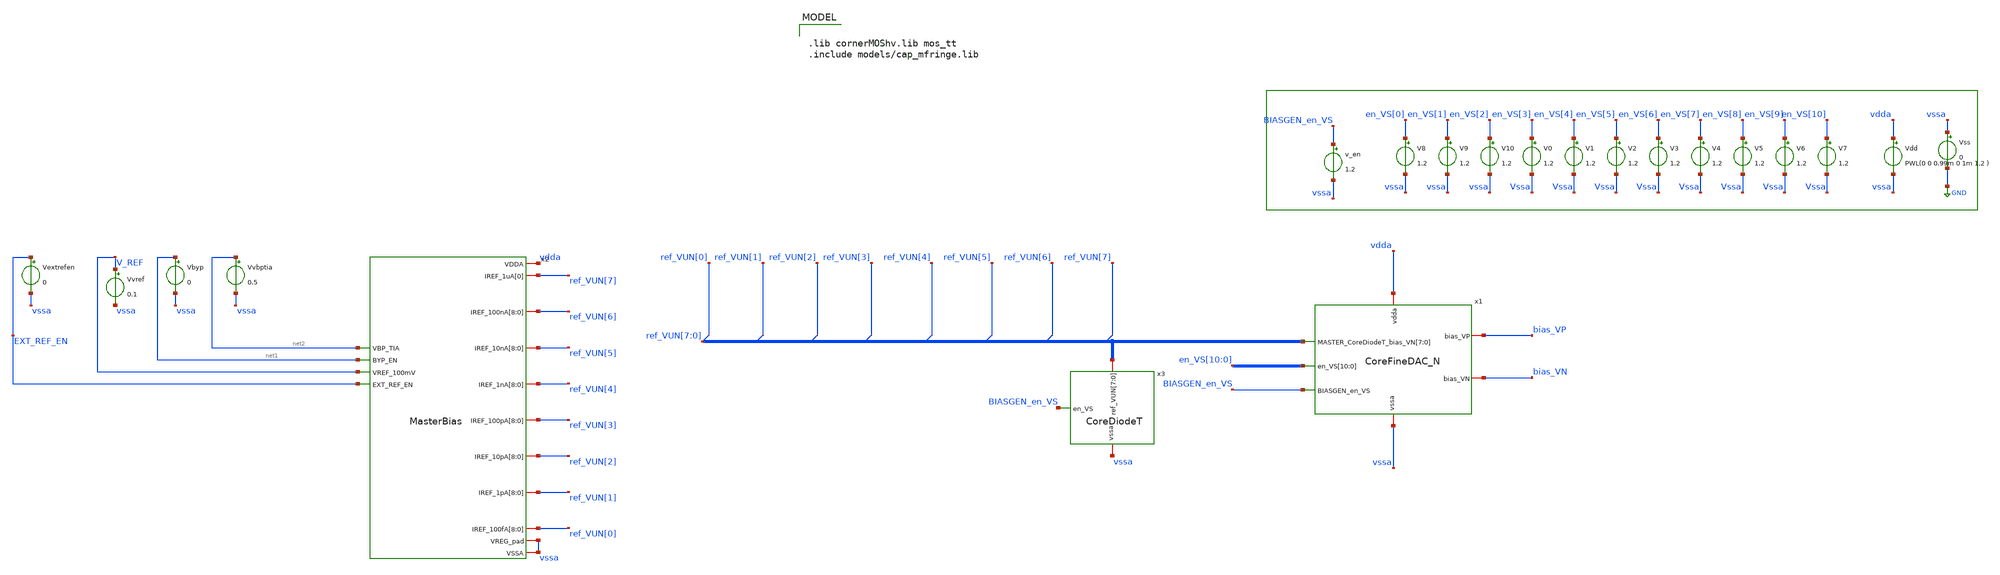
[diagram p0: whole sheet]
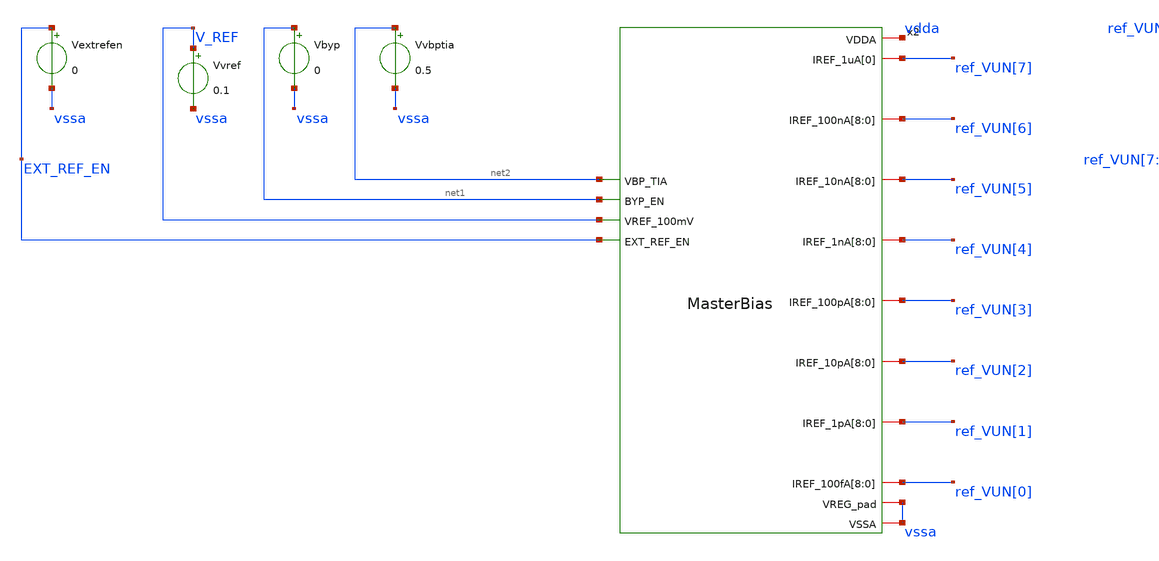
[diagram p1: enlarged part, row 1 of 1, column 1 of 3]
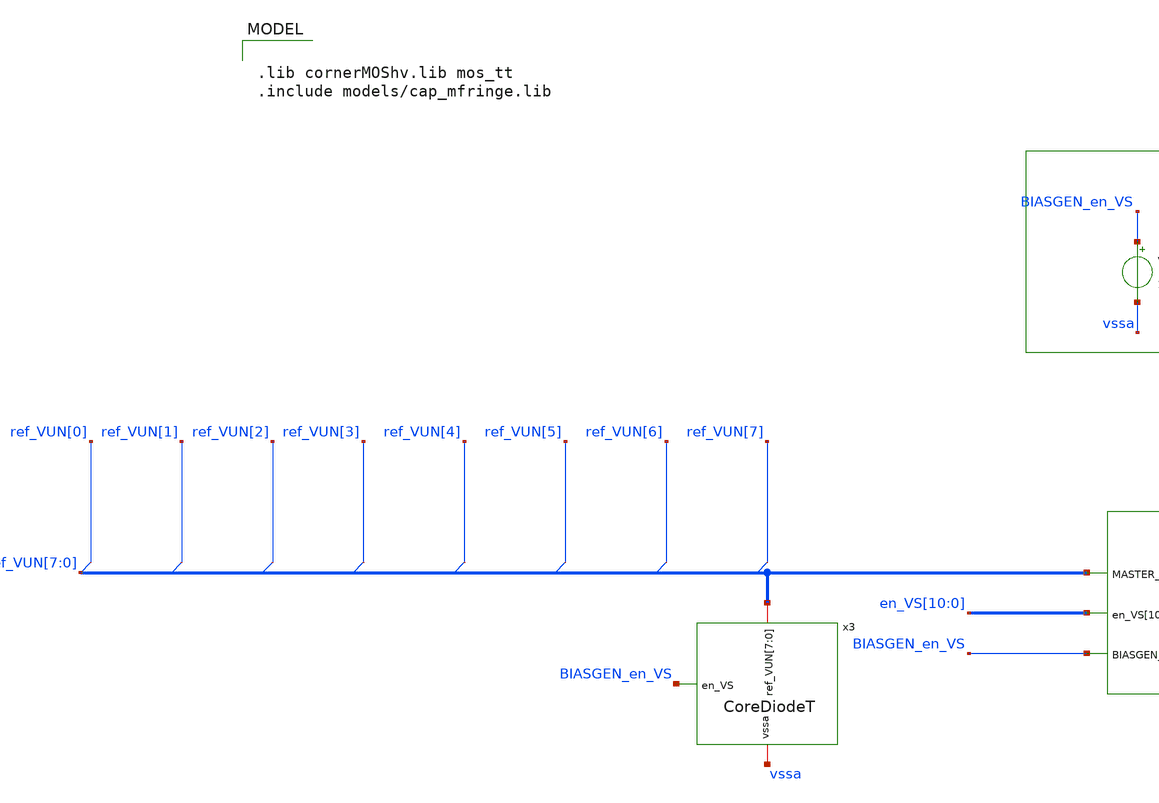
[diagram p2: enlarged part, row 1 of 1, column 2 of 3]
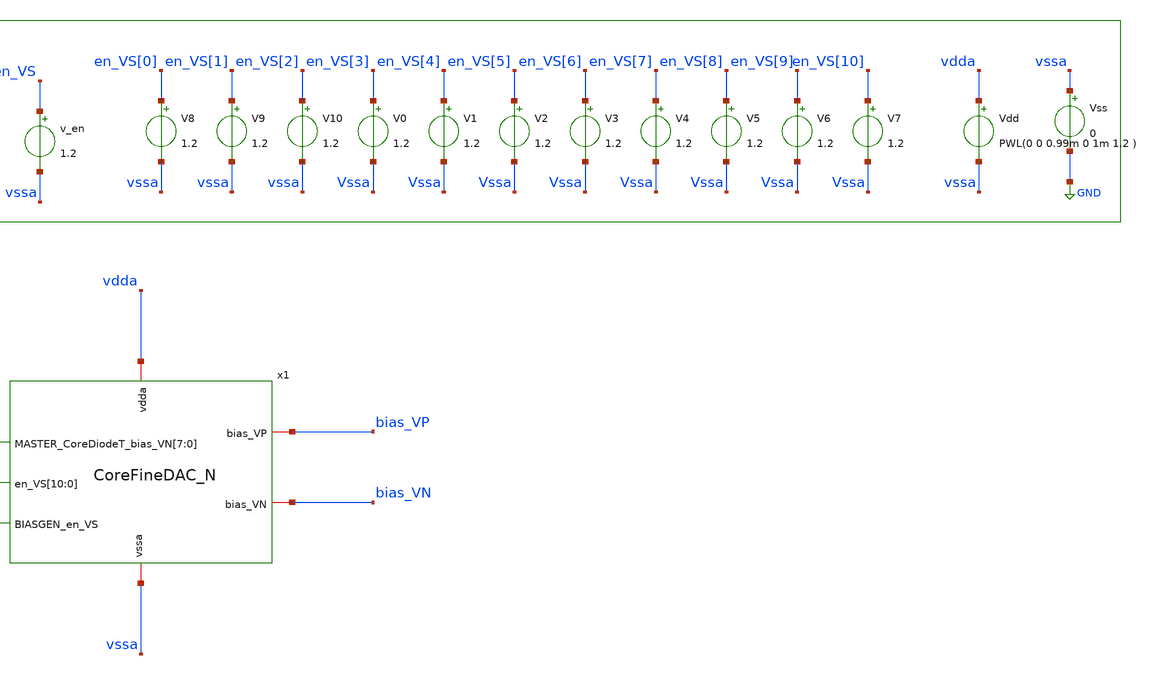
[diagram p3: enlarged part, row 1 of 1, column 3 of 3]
** sch_path: test_bench/CoreFineDAC_N_MasterBiais_tran_tb.sch
**.subckt CoreFineDAC_N_MasterBiais_tran_tb
Vdd vdda vssa PWL(0 0 0.99m 0 1m 1.2 )
V0 en_VS[3] Vssa 1.2
Vss vssa GND 0
V1 en_VS[4] Vssa 1.2
V2 en_VS[5] Vssa 1.2
V3 en_VS[6] Vssa 1.2
V4 en_VS[7] Vssa 1.2
V5 en_VS[8] Vssa 1.2
V6 en_VS[9] Vssa 1.2
V7 en_VS[10] Vssa 1.2
V8 en_VS[0] vssa 1.2
V9 en_VS[1] vssa 1.2
V10 en_VS[2] vssa 1.2
v_en BIASGEN_en_VS vssa 1.2
x1 en_VS[10] en_VS[9] en_VS[8] en_VS[7] en_VS[6] en_VS[5] en_VS[4] en_VS[3] en_VS[2] en_VS[1]
+ en_VS[0] vssa vdda bias_VP bias_VN ref_VUN[7] ref_VUN[6] ref_VUN[5] ref_VUN[4] ref_VUN[3] ref_VUN[2]
+ ref_VUN[1] ref_VUN[0] BIASGEN_en_VS CoreFineDAC_N
x3 ref_VUN[7] ref_VUN[6] ref_VUN[5] ref_VUN[4] ref_VUN[3] ref_VUN[2] ref_VUN[1] ref_VUN[0] vssa
+ BIASGEN_en_VS CoreDiodeT
x2 net2 net1 V_REF EXT_REF_EN vdda ref_VUN[7] ref_VUN[6] ref_VUN[6] ref_VUN[6] ref_VUN[6] ref_VUN[6]
+ ref_VUN[6] ref_VUN[6] ref_VUN[6] ref_VUN[6] ref_VUN[5] ref_VUN[5] ref_VUN[5] ref_VUN[5] ref_VUN[5] ref_VUN[5]
+ ref_VUN[5] ref_VUN[5] ref_VUN[5] ref_VUN[4] ref_VUN[4] ref_VUN[4] ref_VUN[4] ref_VUN[4] ref_VUN[4] ref_VUN[4]
+ ref_VUN[4] ref_VUN[4] ref_VUN[3] ref_VUN[3] ref_VUN[3] ref_VUN[3] ref_VUN[3] ref_VUN[3] ref_VUN[3] ref_VUN[3]
+ ref_VUN[3] ref_VUN[2] ref_VUN[2] ref_VUN[2] ref_VUN[2] ref_VUN[2] ref_VUN[2] ref_VUN[2] ref_VUN[2] ref_VUN[2]
+ ref_VUN[1] ref_VUN[1] ref_VUN[1] ref_VUN[1] ref_VUN[1] ref_VUN[1] ref_VUN[1] ref_VUN[1] ref_VUN[1] ref_VUN[0]
+ ref_VUN[0] ref_VUN[0] ref_VUN[0] ref_VUN[0] ref_VUN[0] ref_VUN[0] ref_VUN[0] ref_VUN[0] vssa vssa MasterBias
Vbyp net1 vssa 0
Vextrefen EXT_REF_EN vssa 0
Vvbptia net2 vssa 0.5
Vvref V_REF vssa 0.1
**** begin user architecture code

.lib cornerMOShv.lib mos_tt
.include models/cap_mfringe.lib



.param temp=27
.options abstol=5e-16
.options gmin=5e-16
.options gmindc=5e-16

.control
let initial_range = 3
let code_range = initial_range
let max_range = 4
while code_range < max_range
    save I(V.x1.V_out_UP) I(V.x1.V_Ibias1) V(x1.V_drain_ISINK) I(V.x1.V_Ibias1)
    + I(V.x3.v_ref_u_0) I(V.x3.v_ref_u_1) I(V.x3.v_ref_u_2) I(V.x3.v_ref_u_3)
    + I(V.x3.v_ref_u_4) I(V.x3.v_ref_u_5) I(V.x3.v_ref_u_6) I(V.x3.v_ref_u_7)
* Set the 3 bits
    alter V8 = 1.2*(code_range % 2)
    alter V9 = 1.2*(floor(code_range/2) % 2)
    alter V10 = 1.2*(floor(code_range/4) % 2)
    let min = 0
    let max = 128
    let code = max-1
    while code < max
      * save all
      * Set the 8 bits
      alter V0 = 1.2*(code % 2)
      alter V1 = 1.2*(floor(code/2) % 2)
      alter V2 = 1.2*(floor(code/4) % 2)
      alter V3 = 1.2*(floor(code/8) % 2)
      alter V4 = 1.2*(floor(code/16) % 2)
      alter V5 = 1.2*(floor(code/32) % 2)
      alter V6 = 1.2*(floor(code/64) % 2)
      alter V7 = 1.2*(floor(code/128) % 2)

      tran 500u 20m

      let digitalCommand[0] = code
      plot I(V.x1.V_out_UP)
      plot I(V.x1.V_Ibias1)
      plot V(x1.V_drain_ISINK)
      plot I(V.x1.V_Ibias1)
      let code = code + 1
      * print code
      write CoreFineDAC_N_MasterBiais_tran_tb/start_up__{$&initial_range}_{$&max}.raw
      write simulations/CoreFineDAC_N_MasterBiais_tran_tb/start_up__{$&initial_range}_{$&max}.raw


   end
   let code_range = code_range + 1
   reset
   * write  simulations/CoreFineDAC_N_MasterBiais_dc_tb/commandRange_{$&initial_range}_{$&max}.raw out_UP
+ V_out_UP V_drain_ISINK_vect
   * write CoreFineDAC_N_MasterBiais_dc_tb/commandRange_{$&initial_range}_{$&max}.raw out_UP
end


.endc





**** end user architecture code
**.ends
.GLOBAL GND
.end
